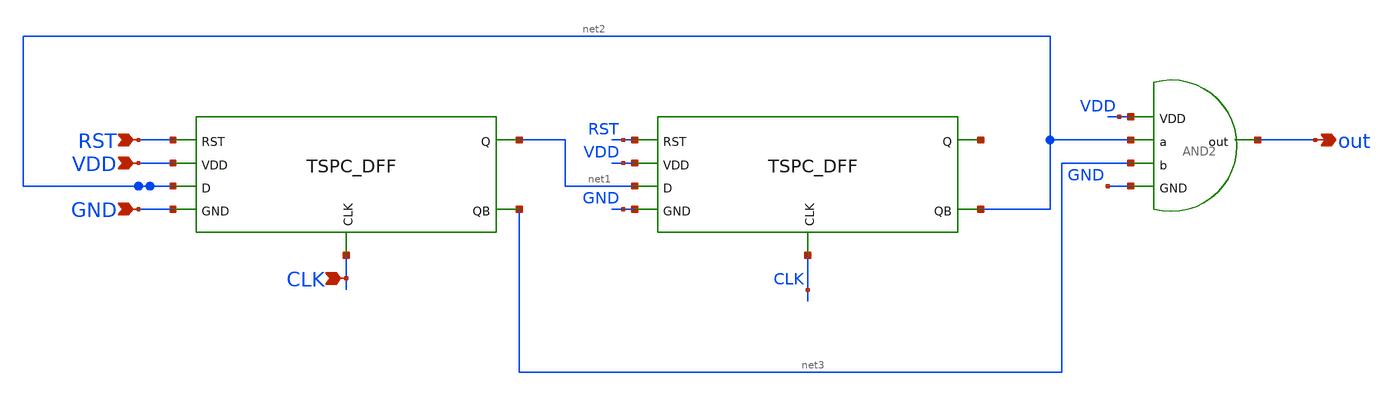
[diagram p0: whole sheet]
** sch_path: blocks/dsp-fft/sch/j_counter.sch
**.subckt j_counter VDD RST GND CLK out
*.ipin VDD
*.ipin RST
*.ipin GND
*.ipin CLK
*.opin out
x1 RST VDD CLK net2 net3 net1 GND tspc_dff
x2 RST VDD CLK net1 net2 net4 GND tspc_dff
x3 VDD net3 net2 out GND AND2
**.ends
.end
